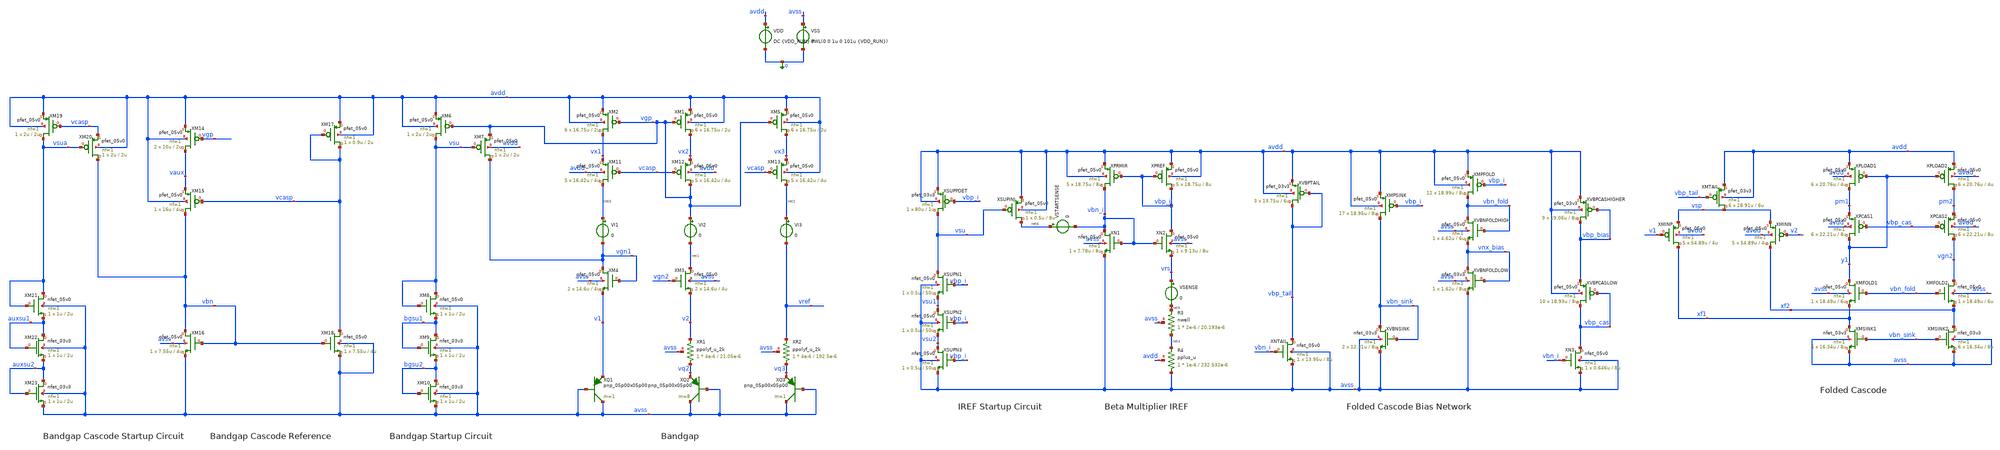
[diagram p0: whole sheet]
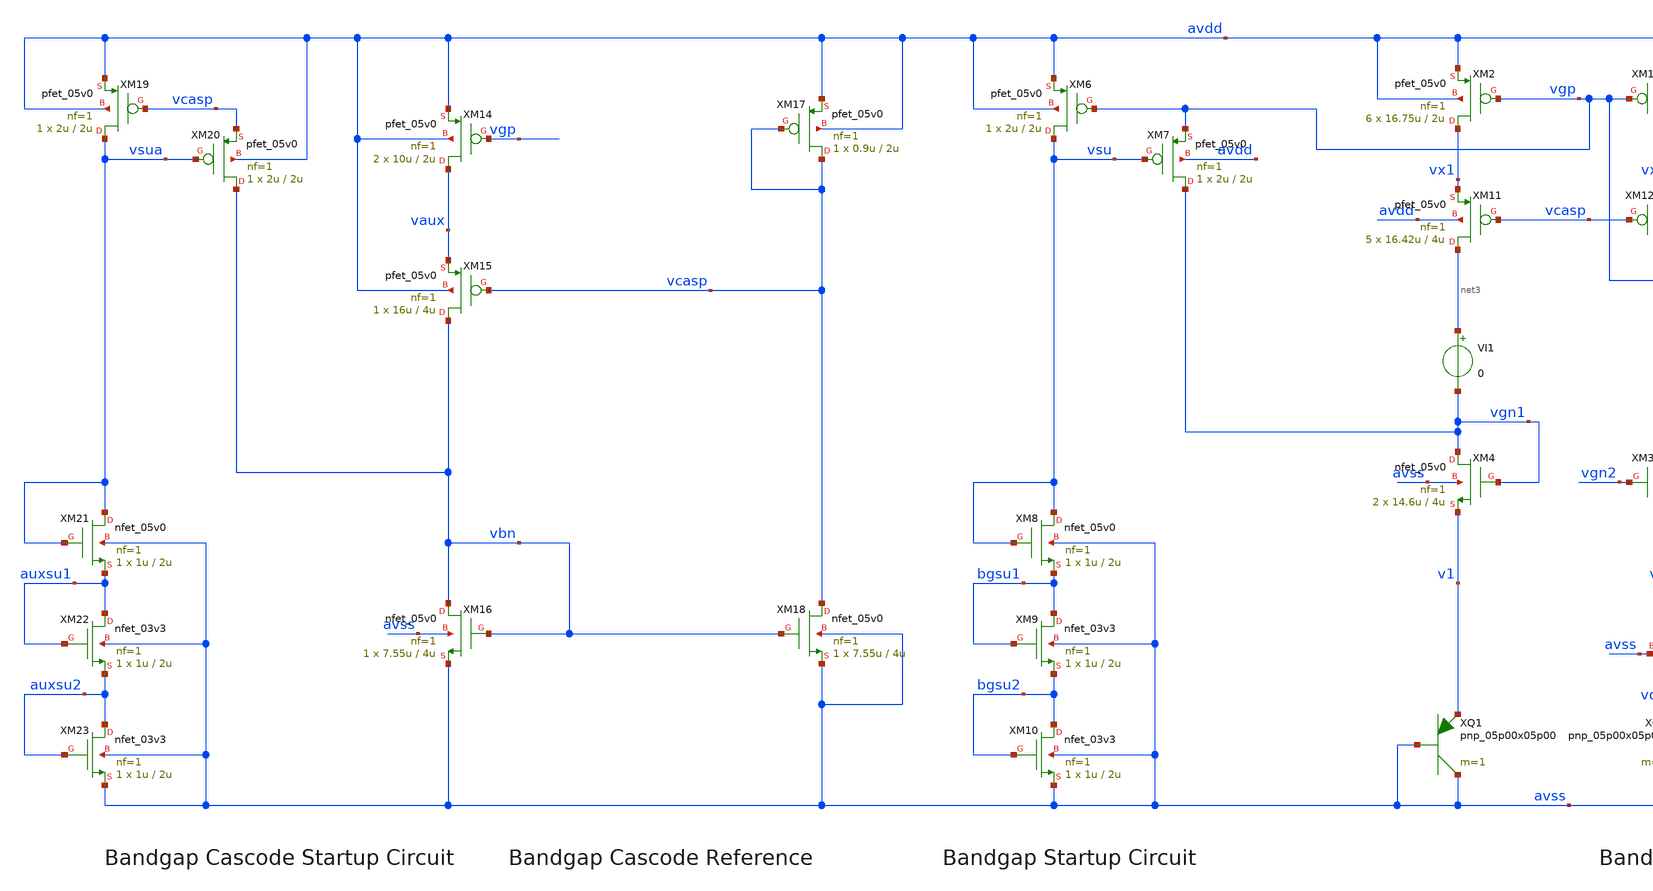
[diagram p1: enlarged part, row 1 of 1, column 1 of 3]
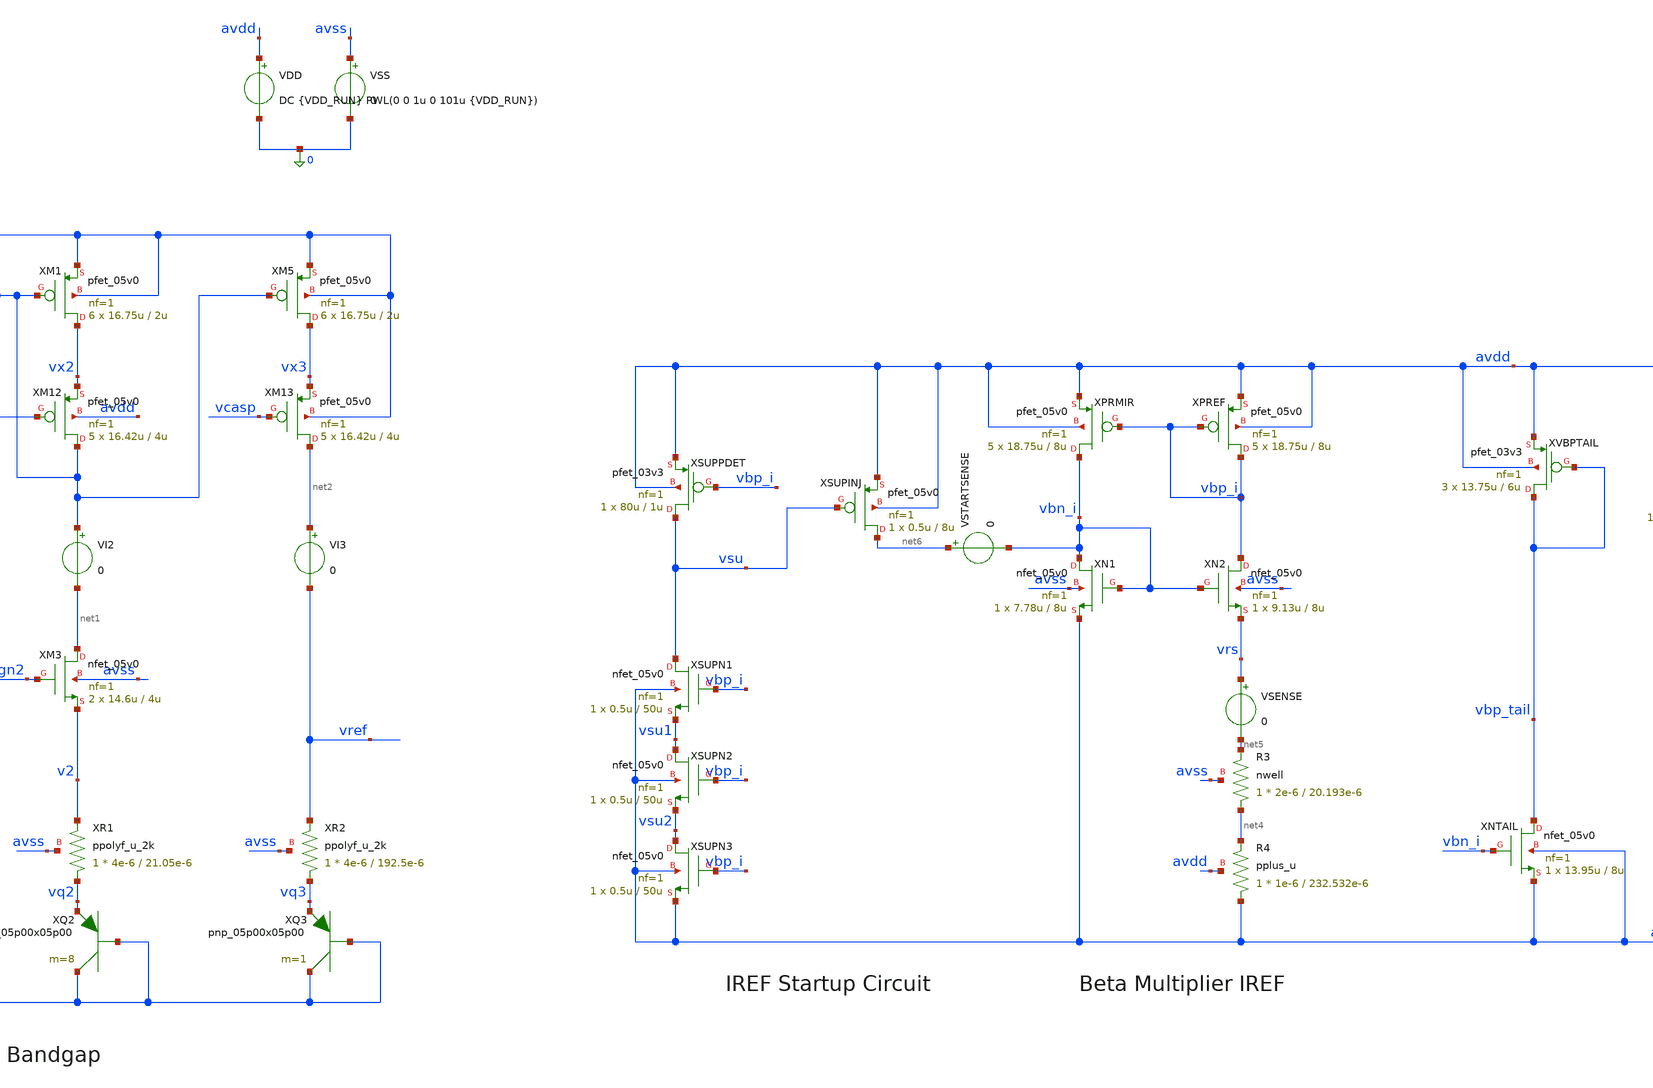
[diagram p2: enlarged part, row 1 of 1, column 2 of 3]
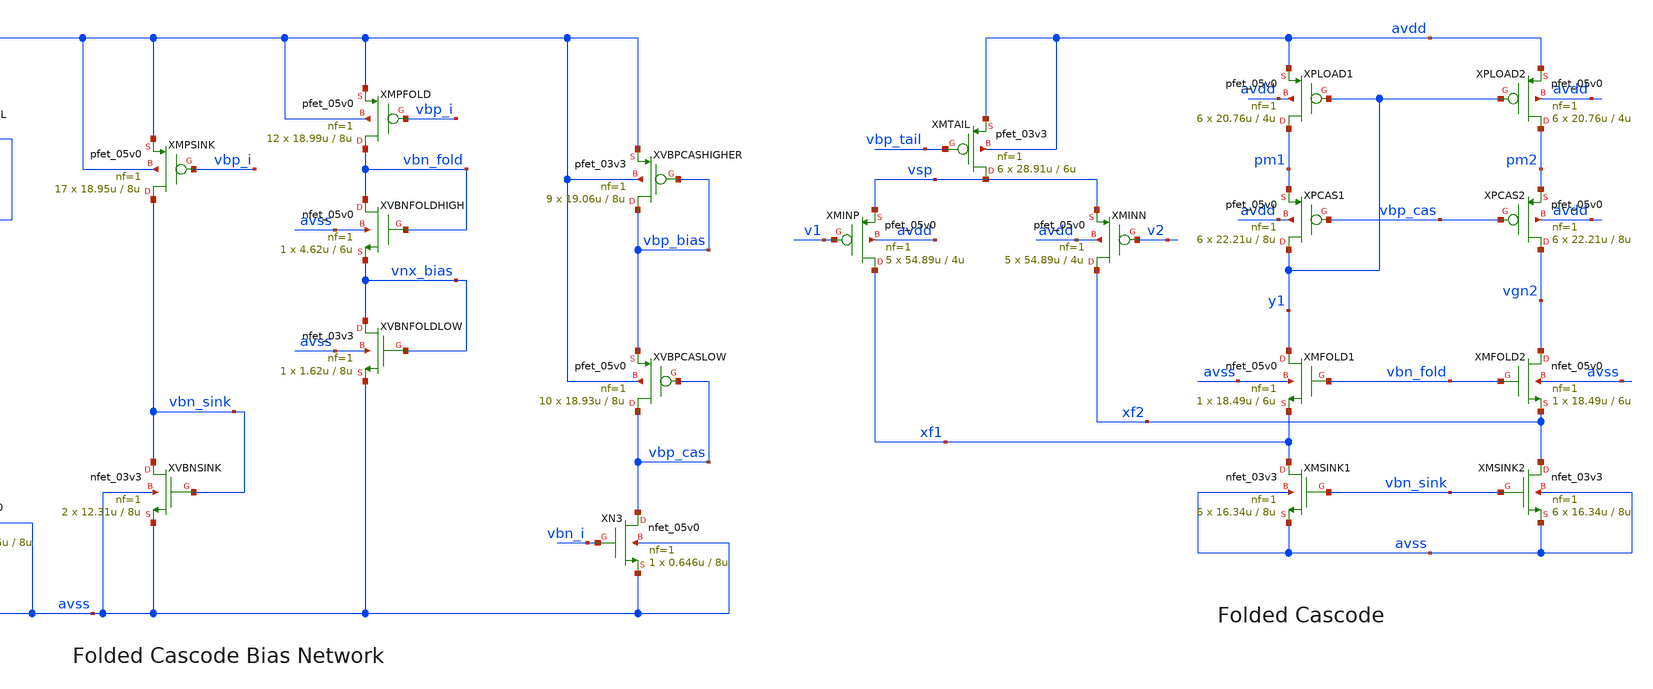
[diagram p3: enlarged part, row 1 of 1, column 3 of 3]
** sch_path: examples/gf180-bandgap/5vfullv2-compatibility.sch
**.subckt 5vfullv2-compatibility
XQ3 avss avss vq3 pnp_05p00x05p00 m=1
XQ2 avss avss vq2 pnp_05p00x05p00 m=8
XQ1 avss avss v1 pnp_05p00x05p00 m=1
XM9 bgsu1 bgsu1 bgsu2 avss nfet_03v3 L=2u W=1u nf=1 ad='int((nf+1)/2) * W/nf * 0.18u' as='int((nf+2)/2) * W/nf * 0.18u'
+ pd='2*int((nf+1)/2) * (W/nf + 0.18u)' ps='2*int((nf+2)/2) * (W/nf + 0.18u)' nrd='0.18u / W' nrs='0.18u / W'
+ sa=0 sb=0 sd=0 m=1
XM10 bgsu2 bgsu2 avss avss nfet_03v3 L=2u W=1u nf=1 ad='int((nf+1)/2) * W/nf * 0.18u' as='int((nf+2)/2) * W/nf * 0.18u'
+ pd='2*int((nf+1)/2) * (W/nf + 0.18u)' ps='2*int((nf+2)/2) * (W/nf + 0.18u)' nrd='0.18u / W' nrs='0.18u / W'
+ sa=0 sb=0 sd=0 m=1
XR1 vq2 v2 avss ppolyf_u_2k r_width=4e-6 r_length=21.05e-6 m=1
XR2 vq3 vref avss ppolyf_u_2k r_width=4e-6 r_length=192.5e-6 m=1
VI1 net3 vgn1 0
VI2 vgp net1 0
VI3 net2 vref 0
XM22 auxsu1 auxsu1 auxsu2 avss nfet_03v3 L=2u W=1u nf=1 ad='int((nf+1)/2) * W/nf * 0.18u' as='int((nf+2)/2) * W/nf * 0.18u'
+ pd='2*int((nf+1)/2) * (W/nf + 0.18u)' ps='2*int((nf+2)/2) * (W/nf + 0.18u)' nrd='0.18u / W' nrs='0.18u / W'
+ sa=0 sb=0 sd=0 m=1
XM23 auxsu2 auxsu2 avss avss nfet_03v3 L=2u W=1u nf=1 ad='int((nf+1)/2) * W/nf * 0.18u' as='int((nf+2)/2) * W/nf * 0.18u'
+ pd='2*int((nf+1)/2) * (W/nf + 0.18u)' ps='2*int((nf+2)/2) * (W/nf + 0.18u)' nrd='0.18u / W' nrs='0.18u / W'
+ sa=0 sb=0 sd=0 m=1
XMTAIL vsp vbp_tail avdd avdd pfet_03v3 L=6u W=28.91u nf=1 ad='int((nf+1)/2) * W/nf * 0.18u' as='int((nf+2)/2) * W/nf * 0.18u'
+ pd='2*int((nf+1)/2) * (W/nf + 0.18u)' ps='2*int((nf+2)/2) * (W/nf + 0.18u)' nrd='0.18u / W' nrs='0.18u / W'
+ sa=0 sb=0 sd=0 m=6
VDD avdd 0 DC {VDD_RUN} PWL(0 0 1u 0 101u {VDD_RUN})
VSS avss 0 0
XMSINK1 xf1 vbn_sink avss avss nfet_03v3 L=8u W=16.34u nf=1 ad='int((nf+1)/2) * W/nf * 0.18u' as='int((nf+2)/2) * W/nf * 0.18u'
+ pd='2*int((nf+1)/2) * (W/nf + 0.18u)' ps='2*int((nf+2)/2) * (W/nf + 0.18u)' nrd='0.18u / W' nrs='0.18u / W'
+ sa=0 sb=0 sd=0 m=6
XMSINK2 xf2 vbn_sink avss avss nfet_03v3 L=8u W=16.34u nf=1 ad='int((nf+1)/2) * W/nf * 0.18u' as='int((nf+2)/2) * W/nf * 0.18u'
+ pd='2*int((nf+1)/2) * (W/nf + 0.18u)' ps='2*int((nf+2)/2) * (W/nf + 0.18u)' nrd='0.18u / W' nrs='0.18u / W'
+ sa=0 sb=0 sd=0 m=6
XR3 net4 net5 avss nwell r_width=2e-6 r_length=20.193e-6 m=1
XR4 avss net4 avdd pplus_u r_width=1e-6 r_length=232.532e-6 m=1
VSENSE vrs net5 0
XSUPPDET vsu vbp_i avdd avdd pfet_03v3 L=1u W=80u nf=1 ad='int((nf+1)/2) * W/nf * 0.18u' as='int((nf+2)/2) * W/nf * 0.18u'
+ pd='2*int((nf+1)/2) * (W/nf + 0.18u)' ps='2*int((nf+2)/2) * (W/nf + 0.18u)' nrd='0.18u / W' nrs='0.18u / W'
+ sa=0 sb=0 sd=0 m=1
VSTARTSENSE net6 vbn_i 0
XPCAS2 vgn2 vbp_cas pm2 avdd pfet_05v0 L=8u W=22.21u nf=1 ad='int((nf+1)/2) * W/nf * 0.18u' as='int((nf+2)/2) * W/nf * 0.18u'
+ pd='2*int((nf+1)/2) * (W/nf + 0.18u)' ps='2*int((nf+2)/2) * (W/nf + 0.18u)' nrd='0.18u / W' nrs='0.18u / W'
+ sa=0 sb=0 sd=0 m=6
XPCAS1 y1 vbp_cas pm1 avdd pfet_05v0 L=8u W=22.21u nf=1 ad='int((nf+1)/2) * W/nf * 0.18u' as='int((nf+2)/2) * W/nf * 0.18u'
+ pd='2*int((nf+1)/2) * (W/nf + 0.18u)' ps='2*int((nf+2)/2) * (W/nf + 0.18u)' nrd='0.18u / W' nrs='0.18u / W'
+ sa=0 sb=0 sd=0 m=6
XMINN xf2 v2 vsp avdd pfet_05v0 L=4u W=54.89u nf=1 ad='int((nf+1)/2) * W/nf * 0.18u' as='int((nf+2)/2) * W/nf * 0.18u'
+ pd='2*int((nf+1)/2) * (W/nf + 0.18u)' ps='2*int((nf+2)/2) * (W/nf + 0.18u)' nrd='0.18u / W' nrs='0.18u / W'
+ sa=0 sb=0 sd=0 m=5
XMINP xf1 v1 vsp avdd pfet_05v0 L=4u W=54.89u nf=1 ad='int((nf+1)/2) * W/nf * 0.18u' as='int((nf+2)/2) * W/nf * 0.18u'
+ pd='2*int((nf+1)/2) * (W/nf + 0.18u)' ps='2*int((nf+2)/2) * (W/nf + 0.18u)' nrd='0.18u / W' nrs='0.18u / W'
+ sa=0 sb=0 sd=0 m=5
XMFOLD2 vgn2 vbn_fold xf2 avss nfet_05v0 L=6u W=18.49u nf=1 ad='int((nf+1)/2) * W/nf * 0.18u' as='int((nf+2)/2) * W/nf * 0.18u'
+ pd='2*int((nf+1)/2) * (W/nf + 0.18u)' ps='2*int((nf+2)/2) * (W/nf + 0.18u)' nrd='0.18u / W' nrs='0.18u / W'
+ sa=0 sb=0 sd=0 m=1
XMFOLD1 y1 vbn_fold xf1 avss nfet_05v0 L=6u W=18.49u nf=1 ad='int((nf+1)/2) * W/nf * 0.18u' as='int((nf+2)/2) * W/nf * 0.18u'
+ pd='2*int((nf+1)/2) * (W/nf + 0.18u)' ps='2*int((nf+2)/2) * (W/nf + 0.18u)' nrd='0.18u / W' nrs='0.18u / W'
+ sa=0 sb=0 sd=0 m=1
XN1 vbn_i vbn_i avss avss nfet_05v0 L=8u W=7.78u nf=1 ad='int((nf+1)/2) * W/nf * 0.18u' as='int((nf+2)/2) * W/nf * 0.18u'
+ pd='2*int((nf+1)/2) * (W/nf + 0.18u)' ps='2*int((nf+2)/2) * (W/nf + 0.18u)' nrd='0.18u / W' nrs='0.18u / W'
+ sa=0 sb=0 sd=0 m=1
XN2 vbp_i vbn_i vrs avss nfet_05v0 L=8u W=9.13u nf=1 ad='int((nf+1)/2) * W/nf * 0.18u' as='int((nf+2)/2) * W/nf * 0.18u'
+ pd='2*int((nf+1)/2) * (W/nf + 0.18u)' ps='2*int((nf+2)/2) * (W/nf + 0.18u)' nrd='0.18u / W' nrs='0.18u / W'
+ sa=0 sb=0 sd=0 m=1
XPREF vbp_i vbp_i avdd avdd pfet_05v0 L=8u W=18.75u nf=1 ad='int((nf+1)/2) * W/nf * 0.18u' as='int((nf+2)/2) * W/nf * 0.18u'
+ pd='2*int((nf+1)/2) * (W/nf + 0.18u)' ps='2*int((nf+2)/2) * (W/nf + 0.18u)' nrd='0.18u / W' nrs='0.18u / W'
+ sa=0 sb=0 sd=0 m=5
XPRMIR vbn_i vbp_i avdd avdd pfet_05v0 L=8u W=18.75u nf=1 ad='int((nf+1)/2) * W/nf * 0.18u' as='int((nf+2)/2) * W/nf * 0.18u'
+ pd='2*int((nf+1)/2) * (W/nf + 0.18u)' ps='2*int((nf+2)/2) * (W/nf + 0.18u)' nrd='0.18u / W' nrs='0.18u / W'
+ sa=0 sb=0 sd=0 m=5
XNTAIL vbp_tail vbn_i avss avss nfet_05v0 L=8u W=13.95u nf=1 ad='int((nf+1)/2) * W/nf * 0.18u' as='int((nf+2)/2) * W/nf * 0.18u'
+ pd='2*int((nf+1)/2) * (W/nf + 0.18u)' ps='2*int((nf+2)/2) * (W/nf + 0.18u)' nrd='0.18u / W' nrs='0.18u / W'
+ sa=0 sb=0 sd=0 m=1
XN3 vbp_cas vbn_i avss avss nfet_05v0 L=8u W=0.646u nf=1 ad='int((nf+1)/2) * W/nf * 0.18u' as='int((nf+2)/2) * W/nf * 0.18u'
+ pd='2*int((nf+1)/2) * (W/nf + 0.18u)' ps='2*int((nf+2)/2) * (W/nf + 0.18u)' nrd='0.18u / W' nrs='0.18u / W'
+ sa=0 sb=0 sd=0 m=1
XMPSINK vbn_sink vbp_i avdd avdd pfet_05v0 L=8u W=18.95u nf=1 ad='int((nf+1)/2) * W/nf * 0.18u' as='int((nf+2)/2) * W/nf * 0.18u'
+ pd='2*int((nf+1)/2) * (W/nf + 0.18u)' ps='2*int((nf+2)/2) * (W/nf + 0.18u)' nrd='0.18u / W' nrs='0.18u / W'
+ sa=0 sb=0 sd=0 m=17
XMPFOLD vbn_fold vbp_i avdd avdd pfet_05v0 L=8u W=18.99u nf=1 ad='int((nf+1)/2) * W/nf * 0.18u' as='int((nf+2)/2) * W/nf * 0.18u'
+ pd='2*int((nf+1)/2) * (W/nf + 0.18u)' ps='2*int((nf+2)/2) * (W/nf + 0.18u)' nrd='0.18u / W' nrs='0.18u / W'
+ sa=0 sb=0 sd=0 m=12
XVBNFOLDHIGH vbn_fold vbn_fold vnx_bias avss nfet_05v0 L=6u W=4.62u nf=1 ad='int((nf+1)/2) * W/nf * 0.18u'
+ as='int((nf+2)/2) * W/nf * 0.18u' pd='2*int((nf+1)/2) * (W/nf + 0.18u)' ps='2*int((nf+2)/2) * (W/nf + 0.18u)'
+ nrd='0.18u / W' nrs='0.18u / W' sa=0 sb=0 sd=0 m=1
XVBPCASLOW vbp_cas vbp_cas vbp_bias avdd pfet_05v0 L=8u W=18.93u nf=1 ad='int((nf+1)/2) * W/nf * 0.18u'
+ as='int((nf+2)/2) * W/nf * 0.18u' pd='2*int((nf+1)/2) * (W/nf + 0.18u)' ps='2*int((nf+2)/2) * (W/nf + 0.18u)'
+ nrd='0.18u / W' nrs='0.18u / W' sa=0 sb=0 sd=0 m=10
XVBNSINK vbn_sink vbn_sink avss avss nfet_03v3 L=8u W=12.31u nf=1 ad='int((nf+1)/2) * W/nf * 0.18u' as='int((nf+2)/2) * W/nf * 0.18u'
+ pd='2*int((nf+1)/2) * (W/nf + 0.18u)' ps='2*int((nf+2)/2) * (W/nf + 0.18u)' nrd='0.18u / W' nrs='0.18u / W'
+ sa=0 sb=0 sd=0 m=2
XVBPTAIL vbp_tail vbp_tail avdd avdd pfet_03v3 L=6u W=13.75u nf=1 ad='int((nf+1)/2) * W/nf * 0.18u' as='int((nf+2)/2) * W/nf * 0.18u'
+ pd='2*int((nf+1)/2) * (W/nf + 0.18u)' ps='2*int((nf+2)/2) * (W/nf + 0.18u)' nrd='0.18u / W' nrs='0.18u / W'
+ sa=0 sb=0 sd=0 m=3
XVBNFOLDLOW vnx_bias vnx_bias avss avss nfet_03v3 L=8u W=1.62u nf=1 ad='int((nf+1)/2) * W/nf * 0.18u'
+ as='int((nf+2)/2) * W/nf * 0.18u' pd='2*int((nf+1)/2) * (W/nf + 0.18u)' ps='2*int((nf+2)/2) * (W/nf + 0.18u)'
+ nrd='0.18u / W' nrs='0.18u / W' sa=0 sb=0 sd=0 m=1
XVBPCASHIGHER vbp_bias vbp_bias avdd avdd pfet_03v3 L=8u W=19.06u nf=1 ad='int((nf+1)/2) * W/nf * 0.18u'
+ as='int((nf+2)/2) * W/nf * 0.18u' pd='2*int((nf+1)/2) * (W/nf + 0.18u)' ps='2*int((nf+2)/2) * (W/nf + 0.18u)'
+ nrd='0.18u / W' nrs='0.18u / W' sa=0 sb=0 sd=0 m=9
XSUPN1 vsu vbp_i vsu1 avss nfet_05v0 L=50u W=0.5u nf=1 ad='int((nf+1)/2) * W/nf * 0.18u' as='int((nf+2)/2) * W/nf * 0.18u'
+ pd='2*int((nf+1)/2) * (W/nf + 0.18u)' ps='2*int((nf+2)/2) * (W/nf + 0.18u)' nrd='0.18u / W' nrs='0.18u / W'
+ sa=0 sb=0 sd=0 m=1
XSUPN2 vsu1 vbp_i vsu2 avss nfet_05v0 L=50u W=0.5u nf=1 ad='int((nf+1)/2) * W/nf * 0.18u' as='int((nf+2)/2) * W/nf * 0.18u'
+ pd='2*int((nf+1)/2) * (W/nf + 0.18u)' ps='2*int((nf+2)/2) * (W/nf + 0.18u)' nrd='0.18u / W' nrs='0.18u / W'
+ sa=0 sb=0 sd=0 m=1
XSUPN3 vsu2 vbp_i avss avss nfet_05v0 L=50u W=0.5u nf=1 ad='int((nf+1)/2) * W/nf * 0.18u' as='int((nf+2)/2) * W/nf * 0.18u'
+ pd='2*int((nf+1)/2) * (W/nf + 0.18u)' ps='2*int((nf+2)/2) * (W/nf + 0.18u)' nrd='0.18u / W' nrs='0.18u / W'
+ sa=0 sb=0 sd=0 m=1
XSUPINJ net6 vsu avdd avdd pfet_05v0 L=8u W=0.5u nf=1 ad='int((nf+1)/2) * W/nf * 0.18u' as='int((nf+2)/2) * W/nf * 0.18u'
+ pd='2*int((nf+1)/2) * (W/nf + 0.18u)' ps='2*int((nf+2)/2) * (W/nf + 0.18u)' nrd='0.18u / W' nrs='0.18u / W'
+ sa=0 sb=0 sd=0 m=1
XM11 net3 vcasp vx1 avdd pfet_05v0 L=4u W=16.42u nf=1 ad='int((nf+1)/2) * W/nf * 0.18u' as='int((nf+2)/2) * W/nf * 0.18u'
+ pd='2*int((nf+1)/2) * (W/nf + 0.18u)' ps='2*int((nf+2)/2) * (W/nf + 0.18u)' nrd='0.18u / W' nrs='0.18u / W'
+ sa=0 sb=0 sd=0 m=5
XM12 vgp vcasp vx2 avdd pfet_05v0 L=4u W=16.42u nf=1 ad='int((nf+1)/2) * W/nf * 0.18u' as='int((nf+2)/2) * W/nf * 0.18u'
+ pd='2*int((nf+1)/2) * (W/nf + 0.18u)' ps='2*int((nf+2)/2) * (W/nf + 0.18u)' nrd='0.18u / W' nrs='0.18u / W'
+ sa=0 sb=0 sd=0 m=5
XM13 net2 vcasp vx3 avdd pfet_05v0 L=4u W=16.42u nf=1 ad='int((nf+1)/2) * W/nf * 0.18u' as='int((nf+2)/2) * W/nf * 0.18u'
+ pd='2*int((nf+1)/2) * (W/nf + 0.18u)' ps='2*int((nf+2)/2) * (W/nf + 0.18u)' nrd='0.18u / W' nrs='0.18u / W'
+ sa=0 sb=0 sd=0 m=5
XM4 vgn1 vgn1 v1 avss nfet_05v0 L=4u W=14.6u nf=1 ad='int((nf+1)/2) * W/nf * 0.18u' as='int((nf+2)/2) * W/nf * 0.18u'
+ pd='2*int((nf+1)/2) * (W/nf + 0.18u)' ps='2*int((nf+2)/2) * (W/nf + 0.18u)' nrd='0.18u / W' nrs='0.18u / W'
+ sa=0 sb=0 sd=0 m=2
XM3 net1 vgn2 v2 avss nfet_05v0 L=4u W=14.6u nf=1 ad='int((nf+1)/2) * W/nf * 0.18u' as='int((nf+2)/2) * W/nf * 0.18u'
+ pd='2*int((nf+1)/2) * (W/nf + 0.18u)' ps='2*int((nf+2)/2) * (W/nf + 0.18u)' nrd='0.18u / W' nrs='0.18u / W'
+ sa=0 sb=0 sd=0 m=2
XM16 vbn vbn avss avss nfet_05v0 L=4u W=7.55u nf=1 ad='int((nf+1)/2) * W/nf * 0.18u' as='int((nf+2)/2) * W/nf * 0.18u'
+ pd='2*int((nf+1)/2) * (W/nf + 0.18u)' ps='2*int((nf+2)/2) * (W/nf + 0.18u)' nrd='0.18u / W' nrs='0.18u / W'
+ sa=0 sb=0 sd=0 m=1
XM18 vcasp vbn avss avss nfet_05v0 L=4u W=7.55u nf=1 ad='int((nf+1)/2) * W/nf * 0.18u' as='int((nf+2)/2) * W/nf * 0.18u'
+ pd='2*int((nf+1)/2) * (W/nf + 0.18u)' ps='2*int((nf+2)/2) * (W/nf + 0.18u)' nrd='0.18u / W' nrs='0.18u / W'
+ sa=0 sb=0 sd=0 m=1
XM15 vbn vcasp vaux avdd pfet_05v0 L=4u W=16u nf=1 ad='int((nf+1)/2) * W/nf * 0.18u' as='int((nf+2)/2) * W/nf * 0.18u'
+ pd='2*int((nf+1)/2) * (W/nf + 0.18u)' ps='2*int((nf+2)/2) * (W/nf + 0.18u)' nrd='0.18u / W' nrs='0.18u / W'
+ sa=0 sb=0 sd=0 m=1
XM17 vcasp vcasp avdd avdd pfet_05v0 L=2u W=0.9u nf=1 ad='int((nf+1)/2) * W/nf * 0.18u' as='int((nf+2)/2) * W/nf * 0.18u'
+ pd='2*int((nf+1)/2) * (W/nf + 0.18u)' ps='2*int((nf+2)/2) * (W/nf + 0.18u)' nrd='0.18u / W' nrs='0.18u / W'
+ sa=0 sb=0 sd=0 m=1
XM6 vsu vgp avdd avdd pfet_05v0 L=2u W=2u nf=1 ad='int((nf+1)/2) * W/nf * 0.18u' as='int((nf+2)/2) * W/nf * 0.18u'
+ pd='2*int((nf+1)/2) * (W/nf + 0.18u)' ps='2*int((nf+2)/2) * (W/nf + 0.18u)' nrd='0.18u / W' nrs='0.18u / W'
+ sa=0 sb=0 sd=0 m=1
XM7 vgn1 vsu vgp avdd pfet_05v0 L=2u W=2u nf=1 ad='int((nf+1)/2) * W/nf * 0.18u' as='int((nf+2)/2) * W/nf * 0.18u'
+ pd='2*int((nf+1)/2) * (W/nf + 0.18u)' ps='2*int((nf+2)/2) * (W/nf + 0.18u)' nrd='0.18u / W' nrs='0.18u / W'
+ sa=0 sb=0 sd=0 m=1
XM19 vsua vcasp avdd avdd pfet_05v0 L=2u W=2u nf=1 ad='int((nf+1)/2) * W/nf * 0.18u' as='int((nf+2)/2) * W/nf * 0.18u'
+ pd='2*int((nf+1)/2) * (W/nf + 0.18u)' ps='2*int((nf+2)/2) * (W/nf + 0.18u)' nrd='0.18u / W' nrs='0.18u / W'
+ sa=0 sb=0 sd=0 m=1
XM20 vbn vsua vcasp avdd pfet_05v0 L=2u W=2u nf=1 ad='int((nf+1)/2) * W/nf * 0.18u' as='int((nf+2)/2) * W/nf * 0.18u'
+ pd='2*int((nf+1)/2) * (W/nf + 0.18u)' ps='2*int((nf+2)/2) * (W/nf + 0.18u)' nrd='0.18u / W' nrs='0.18u / W'
+ sa=0 sb=0 sd=0 m=1
XM8 vsu vsu bgsu1 avss nfet_05v0 L=2u W=1u nf=1 ad='int((nf+1)/2) * W/nf * 0.18u' as='int((nf+2)/2) * W/nf * 0.18u'
+ pd='2*int((nf+1)/2) * (W/nf + 0.18u)' ps='2*int((nf+2)/2) * (W/nf + 0.18u)' nrd='0.18u / W' nrs='0.18u / W'
+ sa=0 sb=0 sd=0 m=1
XM21 vsua vsua auxsu1 avss nfet_05v0 L=2u W=1u nf=1 ad='int((nf+1)/2) * W/nf * 0.18u' as='int((nf+2)/2) * W/nf * 0.18u'
+ pd='2*int((nf+1)/2) * (W/nf + 0.18u)' ps='2*int((nf+2)/2) * (W/nf + 0.18u)' nrd='0.18u / W' nrs='0.18u / W'
+ sa=0 sb=0 sd=0 m=1
XPLOAD1 pm1 y1 avdd avdd pfet_05v0 L=4u W=20.76u nf=1 ad='int((nf+1)/2) * W/nf * 0.18u' as='int((nf+2)/2) * W/nf * 0.18u'
+ pd='2*int((nf+1)/2) * (W/nf + 0.18u)' ps='2*int((nf+2)/2) * (W/nf + 0.18u)' nrd='0.18u / W' nrs='0.18u / W'
+ sa=0 sb=0 sd=0 m=6
XPLOAD2 pm2 y1 avdd avdd pfet_05v0 L=4u W=20.76u nf=1 ad='int((nf+1)/2) * W/nf * 0.18u' as='int((nf+2)/2) * W/nf * 0.18u'
+ pd='2*int((nf+1)/2) * (W/nf + 0.18u)' ps='2*int((nf+2)/2) * (W/nf + 0.18u)' nrd='0.18u / W' nrs='0.18u / W'
+ sa=0 sb=0 sd=0 m=6
XM2 vx1 vgp avdd avdd pfet_05v0 L=2u W=16.75u nf=1 ad='int((nf+1)/2) * W/nf * 0.18u' as='int((nf+2)/2) * W/nf * 0.18u'
+ pd='2*int((nf+1)/2) * (W/nf + 0.18u)' ps='2*int((nf+2)/2) * (W/nf + 0.18u)' nrd='0.18u / W' nrs='0.18u / W'
+ sa=0 sb=0 sd=0 m=6
XM1 vx2 vgp avdd avdd pfet_05v0 L=2u W=16.75u nf=1 ad='int((nf+1)/2) * W/nf * 0.18u' as='int((nf+2)/2) * W/nf * 0.18u'
+ pd='2*int((nf+1)/2) * (W/nf + 0.18u)' ps='2*int((nf+2)/2) * (W/nf + 0.18u)' nrd='0.18u / W' nrs='0.18u / W'
+ sa=0 sb=0 sd=0 m=6
XM5 vx3 vgp avdd avdd pfet_05v0 L=2u W=16.75u nf=1 ad='int((nf+1)/2) * W/nf * 0.18u' as='int((nf+2)/2) * W/nf * 0.18u'
+ pd='2*int((nf+1)/2) * (W/nf + 0.18u)' ps='2*int((nf+2)/2) * (W/nf + 0.18u)' nrd='0.18u / W' nrs='0.18u / W'
+ sa=0 sb=0 sd=0 m=6
XM14 vaux vgp avdd avdd pfet_05v0 L=2u W=10u nf=1 ad='int((nf+1)/2) * W/nf * 0.18u' as='int((nf+2)/2) * W/nf * 0.18u'
+ pd='2*int((nf+1)/2) * (W/nf + 0.18u)' ps='2*int((nf+2)/2) * (W/nf + 0.18u)' nrd='0.18u / W' nrs='0.18u / W'
+ sa=0 sb=0 sd=0 m=2
**** begin user architecture code

* GF180 BANDGAP - SIX-ANALYSIS CROSS-COMPATIBILITY TEST
* Derived from the supplied full V5 5-V testbench; circuit geometry is unchanged.
* 1 startup transient + 3 clean DC sweeps + 1 PSRR AC + 1 output-impedance AC.
* Same nominal model sections and deterministic device settings as the full deck.
* This is a compatibility regression, not full PVT/specification qualification.
* Output files are relative to the chosen simulation directory; no shell commands.

.include /foss/pdks/gf180mcuD/libs.tech/ngspice/design.ngspice
.lib /foss/pdks/gf180mcuD/libs.tech/ngspice/sm141064.ngspice typical
.lib /foss/pdks/gf180mcuD/libs.tech/ngspice/sm141064.ngspice bjt_typical
.lib /foss/pdks/gf180mcuD/libs.tech/ngspice/sm141064.ngspice res_typical

.options tnom=25

.param sw_stat_global=0
.param sw_stat_mismatch=0
.param fnoicor=0

* Current low-TC resistor target.  These parameters are documentary if the
* schematic uses fixed physical lengths.
.param XR1_L_UM=21.05
.param XR2_L_UM=192.50

.param VDD_RUN=5.0
.param P_ILOAD_DC=0
.param P_ILOAD_STEP=0
.param P_ZAC=0

* Testbench-only loads/injection.
ITBLOADDC   vref 0 DC {P_ILOAD_DC}
ITBLOADSTEP vref 0 PWL(0 0 2m 0 2001u {P_ILOAD_STEP} 2500u {P_ILOAD_STEP} 2501u 0)
ITBZ        vref 0 DC 0 AC {P_ZAC}

.control
set noaskquit
set numdgt=12
set wr_vecnames
set wr_singlescale
set filetype=binary

* 1. Real supply-ramp startup at 5 V, 25 C. Keep the original 3 ms horizon.
reset
set temp=25
alter vdd dc=5
alter vdd acmag=0
alter @vdd[pwl] = [ 0 0 1u 0 101u 5 3m 5 ]
alter itbloaddc dc=0
alter @itbloadstep[pwl] = [ 0 0 3m 0 ]
alter itbz acmag=0
save all
tran 100n 3m
let iref_na=abs(i(vsense))*1e9
let idd_ua=-i(vdd)*1e6
let startup_signed_na=i(vstartsense)*1e9
meas tran vref_final avg v(vref) from=2800u to=3000u
meas tran vdd_final avg v(avdd) from=2800u to=3000u
meas tran iref_final_na avg iref_na from=2800u to=3000u
meas tran idd_final_ua avg idd_ua from=2800u to=3000u
meas tran start_leak_na avg startup_signed_na from=2800u to=3000u
write quick-startup.raw v(vref) v(avdd) v(v1) v(v2) i(vsense) i(vdd)
wrdata quick-startup.dat v(vref) v(avdd) iref_na idd_ua startup_signed_na
destroy all

* 2-4. Independent clean DC at temperature endpoints and nominal temperature.
* Each starts from reset -> direct DC; no preceding op/tran in that circuit.
* Seventeen exactly spaced points per sweep cover the required 3.0 to 5.0 V supply range.
foreach t -40 25 125
  reset
  set temp=$t
  alter vdd dc=5
  alter vdd acmag=0
  alter itbloaddc dc=0
  alter itbz acmag=0
  save all
  dc vdd 3.0 5.0 0.125
  let iref_na=abs(i(vsense))*1e9
  let idd_ua=-i(vdd)*1e6
  let verr_uv=(v(v1)-v(v2))*1e6
  meas dc vref_3v find v(vref) at=3
  meas dc vref_5v find v(vref) at=5
  write quick-dc-{$t}C.raw v(vref) v(avdd) v(v1) v(v2) i(vsense) i(vdd)
  wrdata quick-dc-{$t}C.dat v(vref) iref_na idd_ua verr_uv
  destroy all
end

* 5. Nominal PSRR: AC 1 V on VDD, no output injection.
* AC calculates its own bias point; a separate op would be redundant.
reset
set temp=25
alter vdd dc=5
alter vdd acmag=1
alter itbloaddc dc=0
alter itbz acmag=0
save all
ac dec 10 1 1Meg
let psrr_db=-20*log10(mag(v(vref))+1e-30)
meas ac psrr_1hz_db find psrr_db at=1
meas ac psrr_1khz_db find psrr_db at=1k
write quick-psrr.raw v(vref) v(avdd) v(v1) v(v2) i(vsense) i(vdd)
wrdata quick-psrr.dat psrr_db
destroy all

* 6. Nominal closed-loop output impedance: AC 1 A output injection.
reset
set temp=25
alter vdd dc=5
alter vdd acmag=0
alter itbloaddc dc=0
alter itbz acmag=1
save all
ac dec 10 1 1Meg
let zout_ohm=mag(v(vref))
meas ac zout_1hz_ohm find zout_ohm at=1
meas ac zout_1khz_ohm find zout_ohm at=1k
write quick-zout.raw v(vref) v(avdd) v(v1) v(v2) i(vsense) i(vdd)
wrdata quick-zout.dat zout_ohm
destroy all

echo GF180_QUICK_COMPATIBILITY_SIX_ANALYSES_COMPLETE
.endc


**** end user architecture code
**.ends
.end
